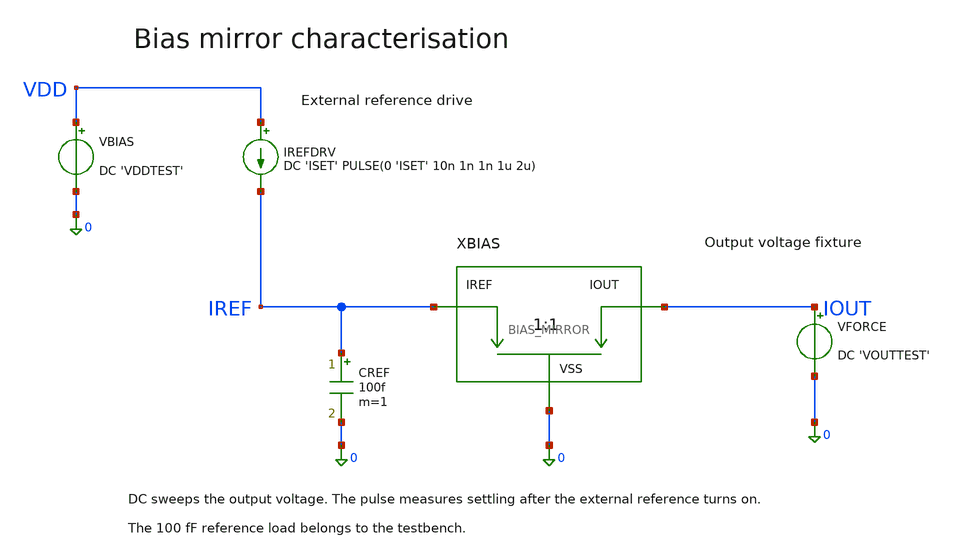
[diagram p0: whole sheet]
** sch_path: examples/sky130-current-mirror/TB_BIAS_MIRROR.sch
**.subckt TB_BIAS_MIRROR
VBIAS VDD 0 DC 'VDDTEST'
IREFDRV VDD IREF DC 'ISET' PULSE(0 'ISET' 10n 1n 1n 1u 2u)
CREF IREF 0 100f m=1
XBIAS IREF IOUT 0 BIAS_MIRROR
VFORCE IOUT 0 DC 'VOUTTEST'
**.ends

* expanding   symbol:  BIAS_MIRROR.sym # of pins=3
** sym_path: examples/sky130-current-mirror/BIAS_MIRROR.sym
** sch_path: examples/sky130-current-mirror/BIAS_MIRROR.sch
.subckt BIAS_MIRROR IREF IOUT VSS
*.ipin IREF
*.opin IOUT
*.iopin VSS
XREF IREF IREF VSS VSS sky130_fd_pr__nfet_01v8 w='MIR_W' l='MIR_L' nf=1 ad='MIR_W*0.30' as='MIR_W*0.30'
+ pd='2*(MIR_W+0.30)' ps='2*(MIR_W+0.30)'
XMIR IOUT IREF VSS VSS sky130_fd_pr__nfet_01v8 w='MIR_W' l='MIR_L' nf=1 ad='MIR_W*0.30' as='MIR_W*0.30'
+ pd='2*(MIR_W+0.30)' ps='2*(MIR_W+0.30)'
.ends

.end
